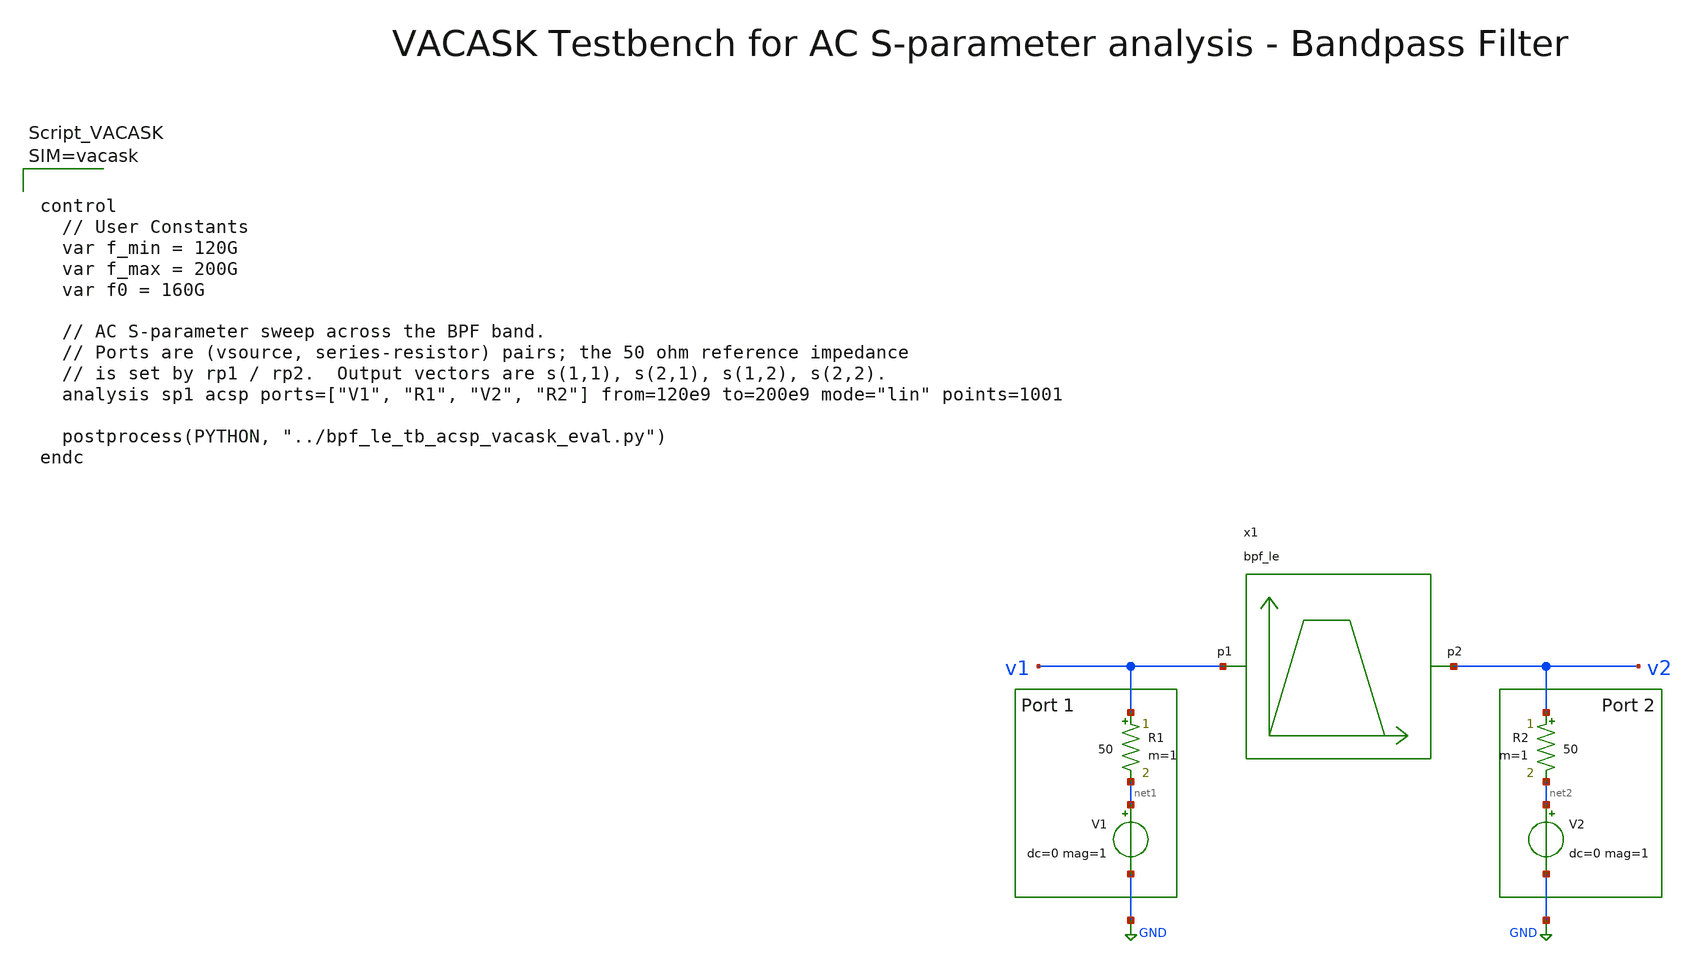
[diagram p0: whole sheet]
** sch_path: testbenches/xschem/bpf_le_tb_acsp_vacask.sch
**.subckt bpf_le_tb_acsp_vacask
x1 v1 v2 bpf_le
R1 v1 net1 50 m=1
V1 net1 GND dc=0 mag=1
R2 v2 net2 50 m=1
V2 net2 GND dc=0 mag=1
**** begin user architecture code






**** end user architecture code
**.ends
.GLOBAL GND
.end
